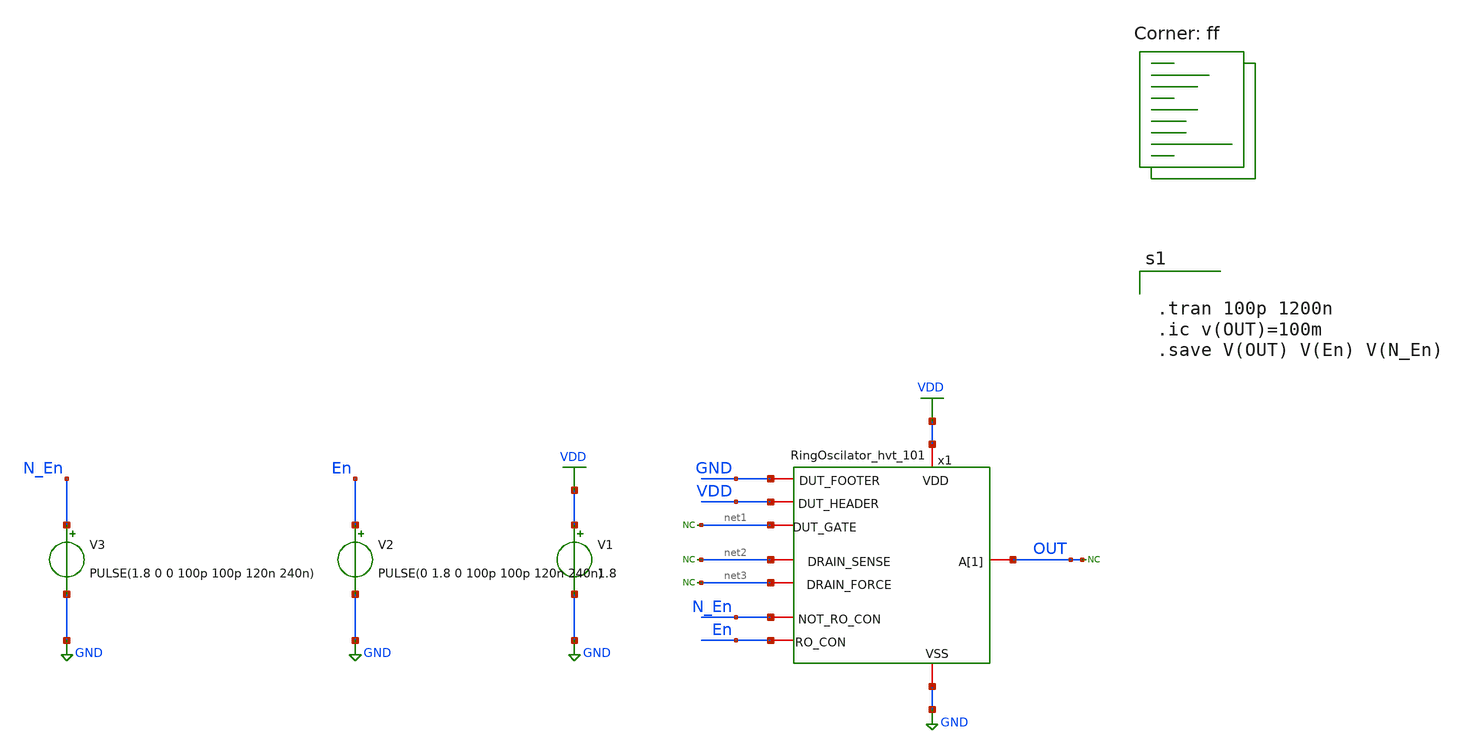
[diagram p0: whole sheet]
** sch_path: HVT/tb_RingOscilator_hvt_101/tb_RingOscilator_hvt_101.sch
**.subckt tb_RingOscilator_hvt_101
V1 VDD GND 1.8
* noconn #net1
* noconn #net2
* noconn #net3
* noconn OUT
V2 En GND PULSE(0 1.8 0 100p 100p 120n 240n)
V3 N_En GND PULSE(1.8 0 0 100p 100p 120n 240n)
x1 GND VDD VDD GND net1 N_En En net2 OUT net3 RingOscilator_hvt_101
**** begin user architecture code
.lib $::SKYWATER_MODELS/sky130.lib.spice ff


.tran 100p 1200n
.ic v(OUT)=100m
.save V(OUT) V(En) V(N_En)


**** end user architecture code
**.ends

* expanding   symbol:
*+  /foss/designs/RO_Aging_UNICASS/HVT/RingOscilator_hvt_101/RingOscilator_hvt_101.sym # of pins=10
** sym_path: HVT/RingOscilator_hvt_101/RingOscilator_hvt_101.sym
** sch_path: HVT/RingOscilator_hvt_101/RingOscilator_hvt_101.sch
.subckt RingOscilator_hvt_101 DUT_FOOTER VDD DUT_HEADER VSS DUT_GATE NOT_RO_CON RO_CON DRAIN_SENSE
+ A[1] DRAIN_FORCE
*.iopin VDD
*.iopin VSS
*.iopin NOT_RO_CON
*.iopin RO_CON
*.iopin DUT_FOOTER
*.iopin DUT_HEADER
*.iopin DUT_GATE
*.iopin DRAIN_SENSE
*.iopin DRAIN_FORCE
*.iopin A[1]
XM3 A[99] A[98] net1 VDD sky130_fd_pr__pfet_01v8_hvt L=0.15 W=0.9 nf=1 ad='int((nf+1)/2) * W/nf * 0.29'
+ as='int((nf+2)/2) * W/nf * 0.29' pd='2*int((nf+1)/2) * (W/nf + 0.29)' ps='2*int((nf+2)/2) * (W/nf + 0.29)'
+ nrd='0.29 / W' nrs='0.29 / W' sa=0 sb=0 sd=0 mult=1 m=1
XM4 net1 NOT_RO_CON VDD VDD sky130_fd_pr__pfet_01v8_hvt L=0.15 W=0.45 nf=1 ad='int((nf+1)/2) * W/nf * 0.29'
+ as='int((nf+2)/2) * W/nf * 0.29' pd='2*int((nf+1)/2) * (W/nf + 0.29)' ps='2*int((nf+2)/2) * (W/nf + 0.29)'
+ nrd='0.29 / W' nrs='0.29 / W' sa=0 sb=0 sd=0 mult=1 m=1
XM7 A[100] A[99] net4 VDD sky130_fd_pr__pfet_01v8_hvt L=0.15 W=0.9 nf=1 ad='int((nf+1)/2) * W/nf * 0.29'
+ as='int((nf+2)/2) * W/nf * 0.29' pd='2*int((nf+1)/2) * (W/nf + 0.29)' ps='2*int((nf+2)/2) * (W/nf + 0.29)'
+ nrd='0.29 / W' nrs='0.29 / W' sa=0 sb=0 sd=0 mult=1 m=1
XM8 net4 DUT_FOOTER VDD VDD sky130_fd_pr__pfet_01v8_hvt L=0.15 W=0.45 nf=1 ad='int((nf+1)/2) * W/nf * 0.29'
+ as='int((nf+2)/2) * W/nf * 0.29' pd='2*int((nf+1)/2) * (W/nf + 0.29)' ps='2*int((nf+2)/2) * (W/nf + 0.29)'
+ nrd='0.29 / W' nrs='0.29 / W' sa=0 sb=0 sd=0 mult=1 m=1
XM10 A[101] A[100] net6 VDD sky130_fd_pr__pfet_01v8_hvt L=0.15 W=0.9 nf=1 ad='int((nf+1)/2) * W/nf * 0.29'
+ as='int((nf+2)/2) * W/nf * 0.29' pd='2*int((nf+1)/2) * (W/nf + 0.29)' ps='2*int((nf+2)/2) * (W/nf + 0.29)'
+ nrd='0.29 / W' nrs='0.29 / W' sa=0 sb=0 sd=0 mult=1 m=1
XM11 net6 NOT_RO_CON VDD VDD sky130_fd_pr__pfet_01v8_hvt L=0.15 W=0.45 nf=1 ad='int((nf+1)/2) * W/nf * 0.29'
+ as='int((nf+2)/2) * W/nf * 0.29' pd='2*int((nf+1)/2) * (W/nf + 0.29)' ps='2*int((nf+2)/2) * (W/nf + 0.29)'
+ nrd='0.29 / W' nrs='0.29 / W' sa=0 sb=0 sd=0 mult=1 m=1
XM1 A[99] A[98] net2 VSS sky130_fd_pr__nfet_01v8 L=0.15 W=0.45 nf=1 ad='int((nf+1)/2) * W/nf * 0.29'
+ as='int((nf+2)/2) * W/nf * 0.29' pd='2*int((nf+1)/2) * (W/nf + 0.29)' ps='2*int((nf+2)/2) * (W/nf + 0.29)'
+ nrd='0.29 / W' nrs='0.29 / W' sa=0 sb=0 sd=0 mult=1 m=1
XM2 net2 RO_CON VSS VSS sky130_fd_pr__nfet_01v8 L=0.15 W=0.45 nf=1 ad='int((nf+1)/2) * W/nf * 0.29' as='int((nf+2)/2) * W/nf * 0.29'
+ pd='2*int((nf+1)/2) * (W/nf + 0.29)' ps='2*int((nf+2)/2) * (W/nf + 0.29)' nrd='0.29 / W' nrs='0.29 / W'
+ sa=0 sb=0 sd=0 mult=1 m=1
XM5 A[100] A[99] net5 VSS sky130_fd_pr__nfet_01v8 L=0.15 W=0.45 nf=1 ad='int((nf+1)/2) * W/nf * 0.29'
+ as='int((nf+2)/2) * W/nf * 0.29' pd='2*int((nf+1)/2) * (W/nf + 0.29)' ps='2*int((nf+2)/2) * (W/nf + 0.29)'
+ nrd='0.29 / W' nrs='0.29 / W' sa=0 sb=0 sd=0 mult=1 m=1
XM6 net5 DUT_HEADER VSS VSS sky130_fd_pr__nfet_01v8 L=0.15 W=0.45 nf=1 ad='int((nf+1)/2) * W/nf * 0.29'
+ as='int((nf+2)/2) * W/nf * 0.29' pd='2*int((nf+1)/2) * (W/nf + 0.29)' ps='2*int((nf+2)/2) * (W/nf + 0.29)'
+ nrd='0.29 / W' nrs='0.29 / W' sa=0 sb=0 sd=0 mult=1 m=1
XM9 A[101] A[100] VSS VSS sky130_fd_pr__nfet_01v8 L=0.15 W=0.45 nf=1 ad='int((nf+1)/2) * W/nf * 0.29'
+ as='int((nf+2)/2) * W/nf * 0.29' pd='2*int((nf+1)/2) * (W/nf + 0.29)' ps='2*int((nf+2)/2) * (W/nf + 0.29)'
+ nrd='0.29 / W' nrs='0.29 / W' sa=0 sb=0 sd=0 mult=1 m=1
x6[1] VDD VSS A[1] A[2] RingStage
x6[2] VDD VSS A[2] A[3] RingStage
x6[3] VDD VSS A[3] A[4] RingStage
x6[4] VDD VSS A[4] A[5] RingStage
x6[5] VDD VSS A[5] A[6] RingStage
x6[6] VDD VSS A[6] A[7] RingStage
x6[7] VDD VSS A[7] A[8] RingStage
x6[8] VDD VSS A[8] A[9] RingStage
x6[9] VDD VSS A[9] A[10] RingStage
x6[10] VDD VSS A[10] A[11] RingStage
x6[11] VDD VSS A[11] A[12] RingStage
x6[12] VDD VSS A[12] A[13] RingStage
x6[13] VDD VSS A[13] A[14] RingStage
x6[14] VDD VSS A[14] A[15] RingStage
x6[15] VDD VSS A[15] A[16] RingStage
x6[16] VDD VSS A[16] A[17] RingStage
x6[17] VDD VSS A[17] A[18] RingStage
x6[18] VDD VSS A[18] A[19] RingStage
x6[19] VDD VSS A[19] A[20] RingStage
x6[20] VDD VSS A[20] A[21] RingStage
x6[21] VDD VSS A[21] A[22] RingStage
x6[22] VDD VSS A[22] A[23] RingStage
x6[23] VDD VSS A[23] A[24] RingStage
x6[24] VDD VSS A[24] A[25] RingStage
x6[25] VDD VSS A[25] A[26] RingStage
x6[26] VDD VSS A[26] A[27] RingStage
x6[27] VDD VSS A[27] A[28] RingStage
x6[28] VDD VSS A[28] A[29] RingStage
x6[29] VDD VSS A[29] A[30] RingStage
x6[30] VDD VSS A[30] A[31] RingStage
x6[31] VDD VSS A[31] A[32] RingStage
x6[32] VDD VSS A[32] A[33] RingStage
x6[33] VDD VSS A[33] A[34] RingStage
x6[34] VDD VSS A[34] A[35] RingStage
x6[35] VDD VSS A[35] A[36] RingStage
x6[36] VDD VSS A[36] A[37] RingStage
x6[37] VDD VSS A[37] A[38] RingStage
x6[38] VDD VSS A[38] A[39] RingStage
x6[39] VDD VSS A[39] A[40] RingStage
x6[40] VDD VSS A[40] A[41] RingStage
x6[41] VDD VSS A[41] A[42] RingStage
x6[42] VDD VSS A[42] A[43] RingStage
x6[43] VDD VSS A[43] A[44] RingStage
x6[44] VDD VSS A[44] A[45] RingStage
x6[45] VDD VSS A[45] A[46] RingStage
x6[46] VDD VSS A[46] A[47] RingStage
x6[47] VDD VSS A[47] A[48] RingStage
x6[48] VDD VSS A[48] A[49] RingStage
x6[49] VDD VSS A[49] A[50] RingStage
x6[50] VDD VSS A[50] A[51] RingStage
x6[51] VDD VSS A[51] A[52] RingStage
x6[52] VDD VSS A[52] A[53] RingStage
x6[53] VDD VSS A[53] A[54] RingStage
x6[54] VDD VSS A[54] A[55] RingStage
x6[55] VDD VSS A[55] A[56] RingStage
x6[56] VDD VSS A[56] A[57] RingStage
x6[57] VDD VSS A[57] A[58] RingStage
x6[58] VDD VSS A[58] A[59] RingStage
x6[59] VDD VSS A[59] A[60] RingStage
x6[60] VDD VSS A[60] A[61] RingStage
x6[61] VDD VSS A[61] A[62] RingStage
x6[62] VDD VSS A[62] A[63] RingStage
x6[63] VDD VSS A[63] A[64] RingStage
x6[64] VDD VSS A[64] A[65] RingStage
x6[65] VDD VSS A[65] A[66] RingStage
x6[66] VDD VSS A[66] A[67] RingStage
x6[67] VDD VSS A[67] A[68] RingStage
x6[68] VDD VSS A[68] A[69] RingStage
x6[69] VDD VSS A[69] A[70] RingStage
x6[70] VDD VSS A[70] A[71] RingStage
x6[71] VDD VSS A[71] A[72] RingStage
x6[72] VDD VSS A[72] A[73] RingStage
x6[73] VDD VSS A[73] A[74] RingStage
x6[74] VDD VSS A[74] A[75] RingStage
x6[75] VDD VSS A[75] A[76] RingStage
x6[76] VDD VSS A[76] A[77] RingStage
x6[77] VDD VSS A[77] A[78] RingStage
x6[78] VDD VSS A[78] A[79] RingStage
x6[79] VDD VSS A[79] A[80] RingStage
x6[80] VDD VSS A[80] A[81] RingStage
x6[81] VDD VSS A[81] A[82] RingStage
x6[82] VDD VSS A[82] A[83] RingStage
x6[83] VDD VSS A[83] A[84] RingStage
x6[84] VDD VSS A[84] A[85] RingStage
x6[85] VDD VSS A[85] A[86] RingStage
x6[86] VDD VSS A[86] A[87] RingStage
x6[87] VDD VSS A[87] A[88] RingStage
x6[88] VDD VSS A[88] A[89] RingStage
x6[89] VDD VSS A[89] A[90] RingStage
x6[90] VDD VSS A[90] A[91] RingStage
x6[91] VDD VSS A[91] A[92] RingStage
x6[92] VDD VSS A[92] A[93] RingStage
x6[93] VDD VSS A[93] A[94] RingStage
x6[94] VDD VSS A[94] A[95] RingStage
x6[95] VDD VSS A[95] A[96] RingStage
x6[96] VDD VSS A[96] A[97] RingStage
x6[97] VDD VSS A[97] A[98] RingStage
x3 VDD VSS A[101] A[1] RingStage
x6 A[99] RO_CON VSS VDD NOT_RO_CON net3 passGate_hvt
x1 A[99] RO_CON VSS VDD NOT_RO_CON DUT_GATE passGate_hvt
x2 A[100] RO_CON VSS VDD NOT_RO_CON DRAIN_FORCE passGate_hvt
x7 A[100] RO_CON VSS VDD NOT_RO_CON DRAIN_SENSE passGate_hvt
x8 A[101] VDD VSS VDD NOT_RO_CON net7 passGate_hvt
x9 A[101] VDD VSS VDD NOT_RO_CON VSS passGate_hvt
.ends


* expanding   symbol:  /foss/designs/UNICASS/RingStage/RingStage.sym # of pins=4
** sym_path: HVT/RingStage/RingStage.sym
** sch_path: HVT/RingStage/RingStage.sch
.subckt RingStage VDD VSS In Out
*.iopin In
*.iopin Out
*.iopin VDD
*.iopin VSS
XM2 Out In VDD VDD sky130_fd_pr__pfet_01v8_hvt L=0.15 W=4.75 nf=1 ad='int((nf+1)/2) * W/nf * 0.29' as='int((nf+2)/2) * W/nf * 0.29'
+ pd='2*int((nf+1)/2) * (W/nf + 0.29)' ps='2*int((nf+2)/2) * (W/nf + 0.29)' nrd='0.29 / W' nrs='0.29 / W'
+ sa=0 sb=0 sd=0 mult=4 m=4
XM1 Out In VSS VSS sky130_fd_pr__nfet_01v8 L=0.15 W=2.1 nf=1 ad='int((nf+1)/2) * W/nf * 0.29' as='int((nf+2)/2) * W/nf * 0.29'
+ pd='2*int((nf+1)/2) * (W/nf + 0.29)' ps='2*int((nf+2)/2) * (W/nf + 0.29)' nrd='0.29 / W' nrs='0.29 / W'
+ sa=0 sb=0 sd=0 mult=2 m=2
XM3 Out VDD net1 VDD sky130_fd_pr__pfet_01v8_hvt L=0.15 W=0.45 nf=1 ad='int((nf+1)/2) * W/nf * 0.29'
+ as='int((nf+2)/2) * W/nf * 0.29' pd='2*int((nf+1)/2) * (W/nf + 0.29)' ps='2*int((nf+2)/2) * (W/nf + 0.29)'
+ nrd='0.29 / W' nrs='0.29 / W' sa=0 sb=0 sd=0 mult=1 m=1
XM4 Out VSS net1 VSS sky130_fd_pr__nfet_01v8 L=0.15 W=0.45 nf=1 ad='int((nf+1)/2) * W/nf * 0.29' as='int((nf+2)/2) * W/nf * 0.29'
+ pd='2*int((nf+1)/2) * (W/nf + 0.29)' ps='2*int((nf+2)/2) * (W/nf + 0.29)' nrd='0.29 / W' nrs='0.29 / W'
+ sa=0 sb=0 sd=0 mult=1 m=1
XM5 Out VDD net2 VDD sky130_fd_pr__pfet_01v8_hvt L=0.15 W=0.45 nf=1 ad='int((nf+1)/2) * W/nf * 0.29'
+ as='int((nf+2)/2) * W/nf * 0.29' pd='2*int((nf+1)/2) * (W/nf + 0.29)' ps='2*int((nf+2)/2) * (W/nf + 0.29)'
+ nrd='0.29 / W' nrs='0.29 / W' sa=0 sb=0 sd=0 mult=1 m=1
XM6 Out VSS net2 VSS sky130_fd_pr__nfet_01v8 L=0.15 W=0.45 nf=1 ad='int((nf+1)/2) * W/nf * 0.29' as='int((nf+2)/2) * W/nf * 0.29'
+ pd='2*int((nf+1)/2) * (W/nf + 0.29)' ps='2*int((nf+2)/2) * (W/nf + 0.29)' nrd='0.29 / W' nrs='0.29 / W'
+ sa=0 sb=0 sd=0 mult=1 m=1
* noconn #net1
* noconn #net2
.ends


* expanding   symbol:  /foss/designs/UNICASS/passGate_hvt/passGate_hvt.sym # of pins=6
** sym_path: HVT/passGate_hvt/passGate_hvt.sym
** sch_path: HVT/passGate_hvt/passGate_hvt.sch
.subckt passGate_hvt In CLKN VSS VDD CLK Out
*.iopin In
*.iopin CLKN
*.iopin Out
*.iopin VSS
*.iopin VDD
*.iopin CLK
XM2 Out CLKN In VDD sky130_fd_pr__pfet_01v8_hvt L=0.15 W=0.45 nf=1 ad='int((nf+1)/2) * W/nf * 0.29' as='int((nf+2)/2) * W/nf * 0.29'
+ pd='2*int((nf+1)/2) * (W/nf + 0.29)' ps='2*int((nf+2)/2) * (W/nf + 0.29)' nrd='0.29 / W' nrs='0.29 / W'
+ sa=0 sb=0 sd=0 mult=1 m=1
XM1 Out CLK In VSS sky130_fd_pr__nfet_01v8 L=0.15 W=0.45 nf=1 ad='int((nf+1)/2) * W/nf * 0.29' as='int((nf+2)/2) * W/nf * 0.29'
+ pd='2*int((nf+1)/2) * (W/nf + 0.29)' ps='2*int((nf+2)/2) * (W/nf + 0.29)' nrd='0.29 / W' nrs='0.29 / W'
+ sa=0 sb=0 sd=0 mult=1 m=1
.ends

.GLOBAL VDD
.GLOBAL GND
.end
